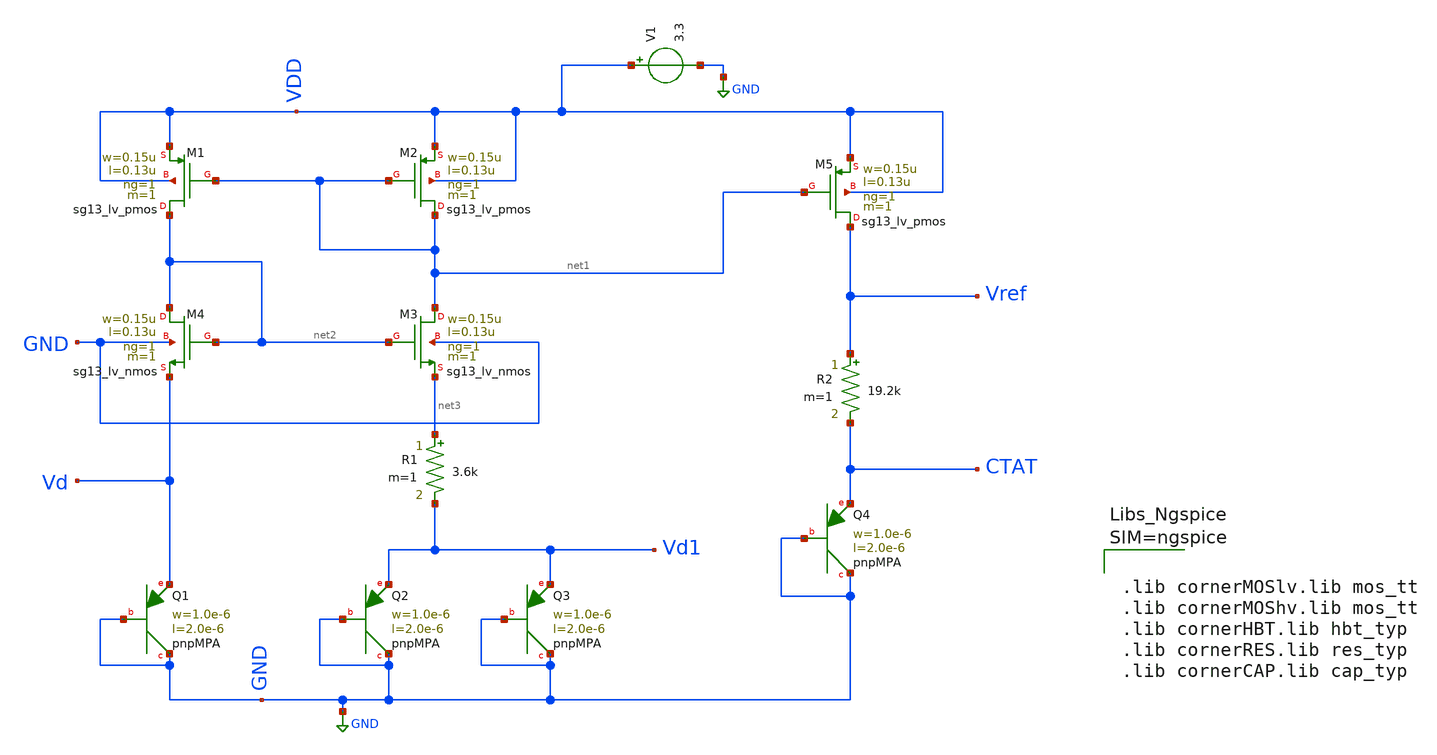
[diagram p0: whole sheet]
** sch_path: bgr_schematic.sch
**.subckt bgr_schematic
XM1 net2 net1 VDD VDD sg13_lv_pmos w=0.15u l=0.13u ng=1 m=1 mm_ok=1
XM2 net1 net1 VDD VDD sg13_lv_pmos w=0.15u l=0.13u ng=1 m=1 mm_ok=1
XM3 net1 net2 net3 GND sg13_lv_nmos w=0.15u l=0.13u ng=1 m=1 mm_ok=1
XM4 net2 net2 Vd GND sg13_lv_nmos w=0.15u l=0.13u ng=1 m=1 mm_ok=1
R1 net3 Vd1 3.6k m=1
XQ1 GND GND Vd pnpMPA a=2p p=6u m=1
XQ2 GND GND Vd1 pnpMPA a=2p p=6u m=1
XQ3 GND GND Vd1 pnpMPA a=2p p=6u m=8
XM5 Vref net1 VDD VDD sg13_lv_pmos w=0.15u l=0.13u ng=1 m=1 mm_ok=1
R2 Vref CTAT 19.2k m=1
XQ4 GND GND CTAT pnpMPA a=2p p=6u m=1
V1 VDD GND 3.3
**** begin user architecture code



.lib cornerMOSlv.lib mos_tt
.lib cornerMOShv.lib mos_tt
.lib cornerHBT.lib hbt_typ
.lib cornerRES.lib res_typ
.lib cornerCAP.lib cap_typ



**** end user architecture code
**.ends
.GLOBAL GND
.end
